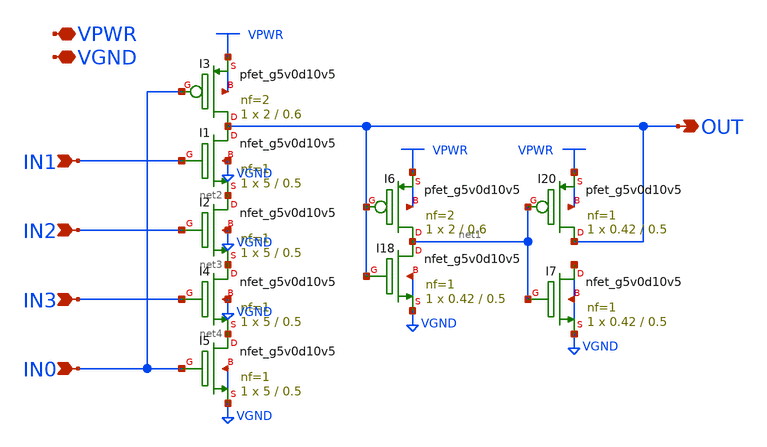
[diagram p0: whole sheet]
** sch_path: gpiov2_amux_nand4.sch
* Copyright 2023 David Mitchell Bailey
* Licensed under the Apache License, Version 2.0 (the "License");
* you may not use this file except in compliance with the License.
* You may obtain a copy of the License at
* https://www.apache.org/licenses/LICENSE-2.0
* Unless required by applicable law or agreed to in writing, software
* distributed under the License is distributed on an "AS IS" BASIS,
* WITHOUT WARRANTIES OR CONDITIONS OF ANY KIND, either express or implied.
* See the License for the specific language governing permissions and
* limitations under the License.
**.subckt gpiov2_amux_nand4 IN1 VPWR VGND IN2 IN0 IN3 OUT
*.ipin IN1
*.iopin VPWR
*.iopin VGND
*.ipin IN2
*.ipin IN0
*.ipin IN3
*.opin OUT
XI1 OUT IN1 net2 VGND sky130_fd_pr__nfet_g5v0d10v5 L=0.5 W=5 nf=1 ad='int((nf+1)/2) * W/nf * 0.29' as='int((nf+2)/2) * W/nf * 0.29'
+ pd='2*int((nf+1)/2) * (W/nf + 0.29)' ps='2*int((nf+2)/2) * (W/nf + 0.29)' nrd='0.29 / W' nrs='0.29 / W'
+ sa=0 sb=0 sd=0 mult=1 m=1
XI3 OUT IN0 VPWR VPWR sky130_fd_pr__pfet_g5v0d10v5 L=0.6 W=2 nf=2 ad='int((nf+1)/2) * W/nf * 0.29' as='int((nf+2)/2) * W/nf * 0.29'
+ pd='2*int((nf+1)/2) * (W/nf + 0.29)' ps='2*int((nf+2)/2) * (W/nf + 0.29)' nrd='0.29 / W' nrs='0.29 / W'
+ sa=0 sb=0 sd=0 mult=1 m=1
XI2 net2 IN2 net3 VGND sky130_fd_pr__nfet_g5v0d10v5 L=0.5 W=5 nf=1 ad='int((nf+1)/2) * W/nf * 0.29' as='int((nf+2)/2) * W/nf * 0.29'
+ pd='2*int((nf+1)/2) * (W/nf + 0.29)' ps='2*int((nf+2)/2) * (W/nf + 0.29)' nrd='0.29 / W' nrs='0.29 / W'
+ sa=0 sb=0 sd=0 mult=1 m=1
XI4 net3 IN3 net4 VGND sky130_fd_pr__nfet_g5v0d10v5 L=0.5 W=5 nf=1 ad='int((nf+1)/2) * W/nf * 0.29' as='int((nf+2)/2) * W/nf * 0.29'
+ pd='2*int((nf+1)/2) * (W/nf + 0.29)' ps='2*int((nf+2)/2) * (W/nf + 0.29)' nrd='0.29 / W' nrs='0.29 / W'
+ sa=0 sb=0 sd=0 mult=1 m=1
XI5 net4 IN0 VGND VGND sky130_fd_pr__nfet_g5v0d10v5 L=0.5 W=5 nf=1 ad='int((nf+1)/2) * W/nf * 0.29' as='int((nf+2)/2) * W/nf * 0.29'
+ pd='2*int((nf+1)/2) * (W/nf + 0.29)' ps='2*int((nf+2)/2) * (W/nf + 0.29)' nrd='0.29 / W' nrs='0.29 / W'
+ sa=0 sb=0 sd=0 mult=1 m=1
XI18 net1 OUT VGND VGND sky130_fd_pr__nfet_g5v0d10v5 L=0.5 W=0.42 nf=1 ad='int((nf+1)/2) * W/nf * 0.29'
+ as='int((nf+2)/2) * W/nf * 0.29' pd='2*int((nf+1)/2) * (W/nf + 0.29)' ps='2*int((nf+2)/2) * (W/nf + 0.29)'
+ nrd='0.29 / W' nrs='0.29 / W' sa=0 sb=0 sd=0 mult=1 m=1
XI6 net1 OUT VPWR VPWR sky130_fd_pr__pfet_g5v0d10v5 L=0.6 W=2 nf=2 ad='int((nf+1)/2) * W/nf * 0.29' as='int((nf+2)/2) * W/nf * 0.29'
+ pd='2*int((nf+1)/2) * (W/nf + 0.29)' ps='2*int((nf+2)/2) * (W/nf + 0.29)' nrd='0.29 / W' nrs='0.29 / W'
+ sa=0 sb=0 sd=0 mult=1 m=1
XI7 VGND net1 VGND VGND sky130_fd_pr__nfet_g5v0d10v5 L=0.5 W=0.42 nf=1 ad='int((nf+1)/2) * W/nf * 0.29'
+ as='int((nf+2)/2) * W/nf * 0.29' pd='2*int((nf+1)/2) * (W/nf + 0.29)' ps='2*int((nf+2)/2) * (W/nf + 0.29)'
+ nrd='0.29 / W' nrs='0.29 / W' sa=0 sb=0 sd=0 mult=1 m=1
XI20 OUT net1 VPWR VPWR sky130_fd_pr__pfet_g5v0d10v5 L=0.5 W=0.42 nf=1 ad='int((nf+1)/2) * W/nf * 0.29'
+ as='int((nf+2)/2) * W/nf * 0.29' pd='2*int((nf+1)/2) * (W/nf + 0.29)' ps='2*int((nf+2)/2) * (W/nf + 0.29)'
+ nrd='0.29 / W' nrs='0.29 / W' sa=0 sb=0 sd=0 mult=1 m=1
**.ends
.end
